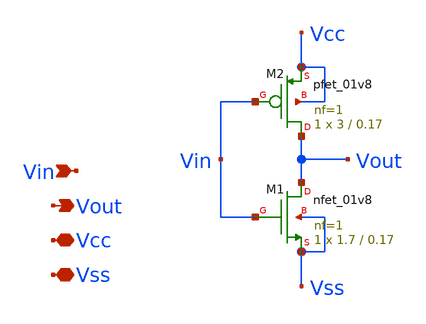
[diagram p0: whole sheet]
** sch_path: Git Files/Simulation Schematic/Pre Emphasis Driver/Buf1/inv1.sch
**.subckt inv1 Vin Vout Vcc Vss
*.ipin Vin
*.opin Vout
*.iopin Vcc
*.iopin Vss
XM1 Vout Vin Vss Vss sky130_fd_pr__nfet_01v8 L=0.17 W=1.7 nf=1 ad='int((nf+1)/2) * W/nf * 0.29' as='int((nf+2)/2) * W/nf * 0.29'
+ pd='2*int((nf+1)/2) * (W/nf + 0.29)' ps='2*int((nf+2)/2) * (W/nf + 0.29)' nrd='0.29 / W' nrs='0.29 / W'
+ sa=0 sb=0 sd=0 mult=1 m=1
XM2 Vout Vin Vcc Vcc sky130_fd_pr__pfet_01v8 L=0.17 W=3 nf=1 ad='int((nf+1)/2) * W/nf * 0.29' as='int((nf+2)/2) * W/nf * 0.29'
+ pd='2*int((nf+1)/2) * (W/nf + 0.29)' ps='2*int((nf+2)/2) * (W/nf + 0.29)' nrd='0.29 / W' nrs='0.29 / W'
+ sa=0 sb=0 sd=0 mult=1 m=1
**.ends
.end
